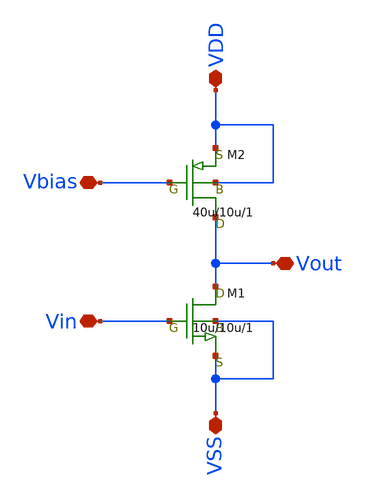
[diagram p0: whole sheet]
** sch_path: common-source-amplifier.sch
**.subckt common-source-amplifier Vout Vbias Vin VDD VSS
*.iopin Vout
*.iopin Vbias
*.iopin Vin
*.iopin VDD
*.iopin VSS
M2 Vout Vbias VDD VDD pch w=40u l=10u as=0 ps=0 ad=0 pd=0 m=1
M1 Vout Vin VSS VSS nch w=10u l=10u as=0 ps=0 ad=0 pd=0 m=1
**.ends
.end
